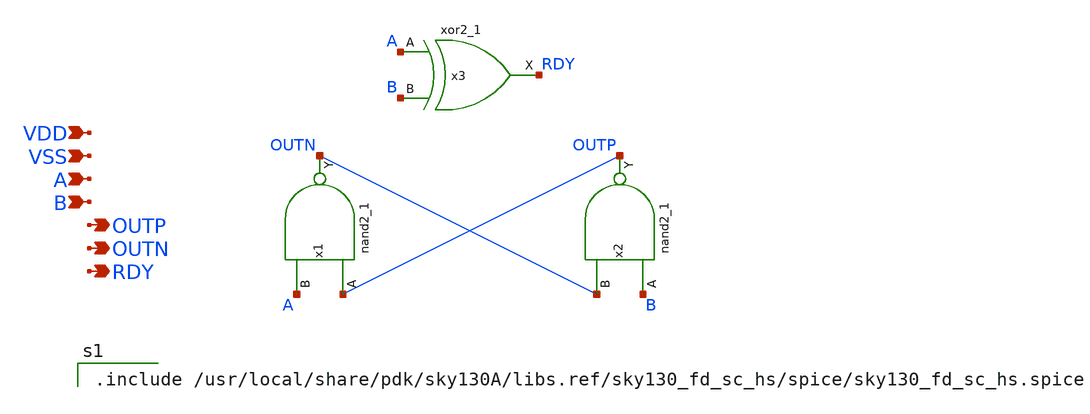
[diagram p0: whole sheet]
** sch_path: xschem/pd_out.sch
**.subckt pd_out OUTN OUTP RDY A B VSS VDD
*.opin OUTN
*.opin OUTP
*.opin RDY
*.ipin A
*.ipin B
*.ipin VSS
*.ipin VDD
x1 OUTP A VSS VSS VDD VDD OUTN sky130_fd_sc_hs__nand2_1
x2 B OUTN VSS VSS VDD VDD OUTP sky130_fd_sc_hs__nand2_1
x3 A B VSS VSS VDD VDD RDY sky130_fd_sc_hs__xor2_1
**** begin user architecture code

.include /usr/local/share/pdk/sky130A/libs.ref/sky130_fd_sc_hs/spice/sky130_fd_sc_hs.spice

**** end user architecture code
**.ends
.end
